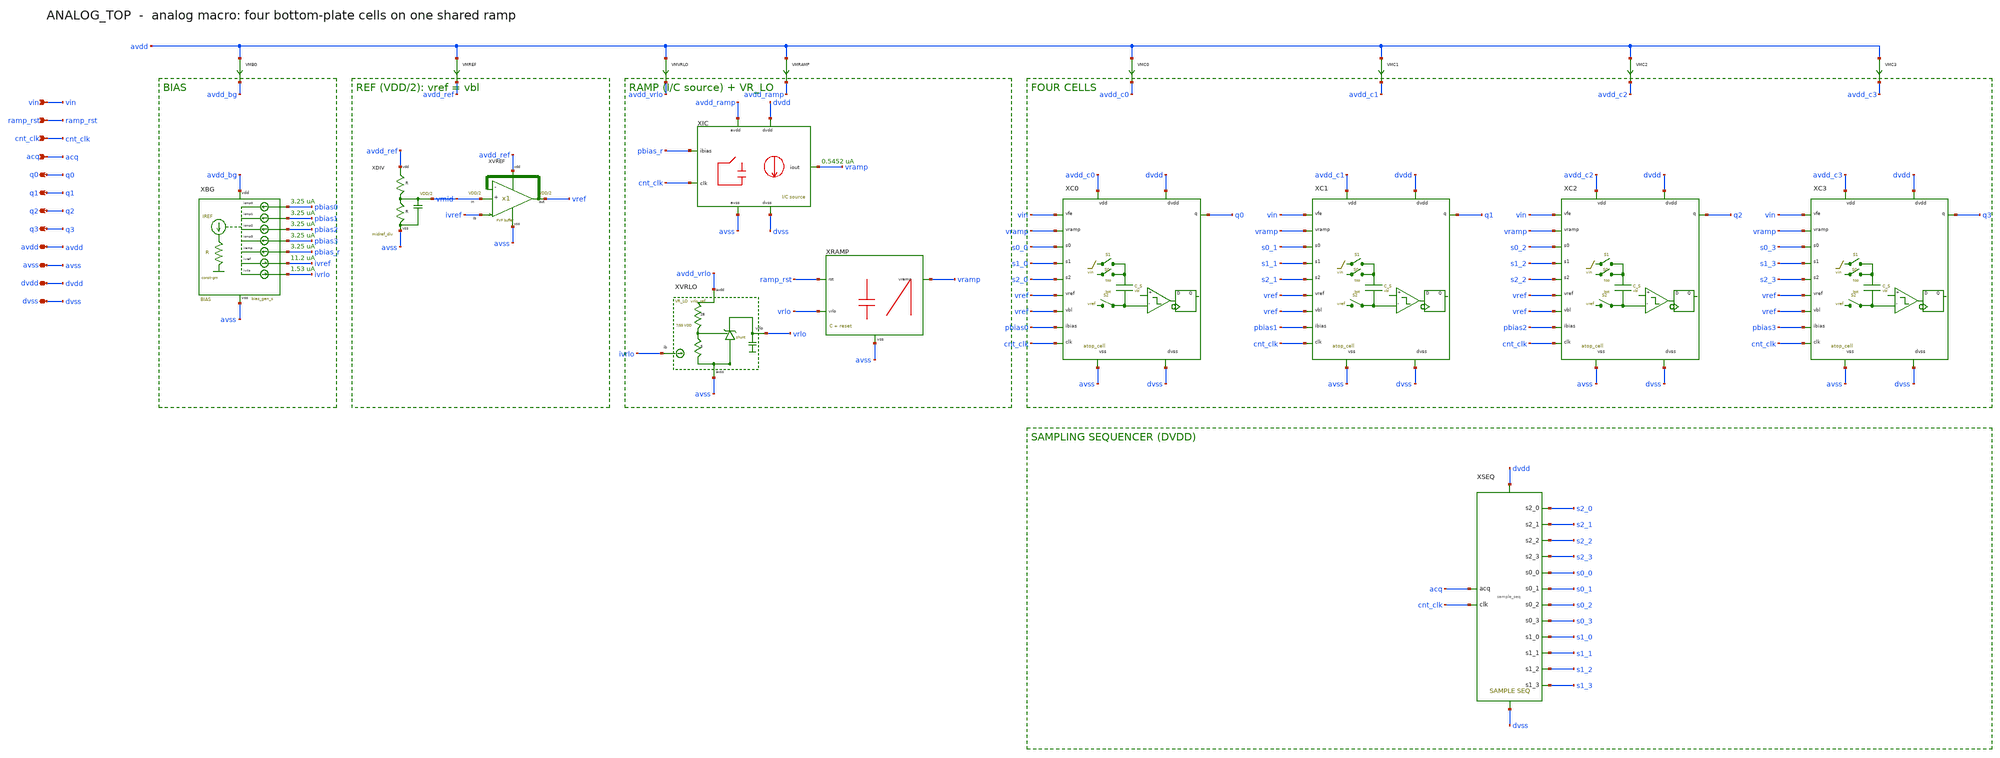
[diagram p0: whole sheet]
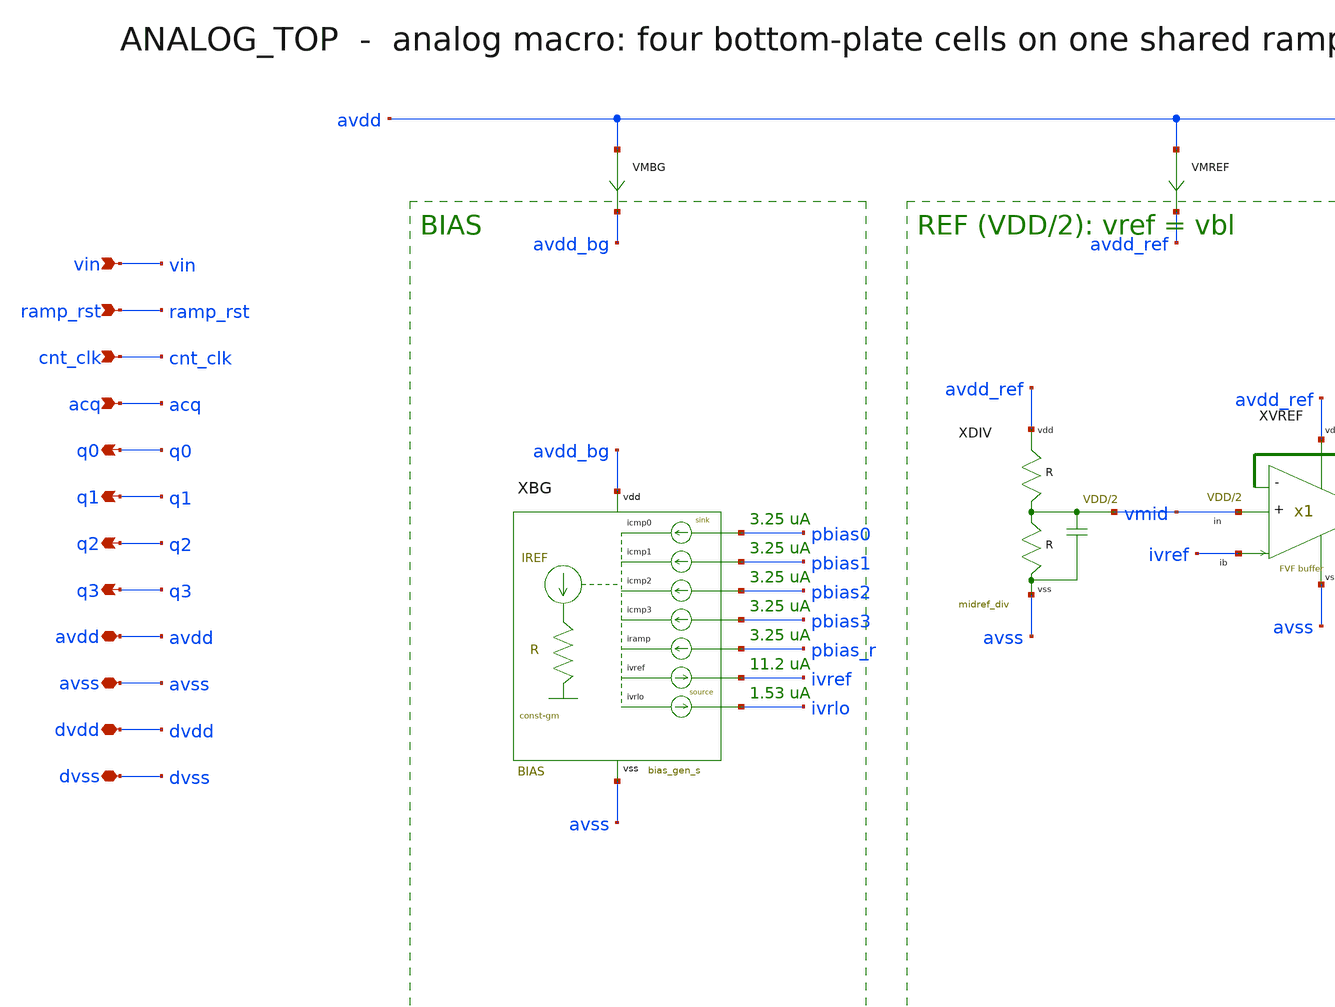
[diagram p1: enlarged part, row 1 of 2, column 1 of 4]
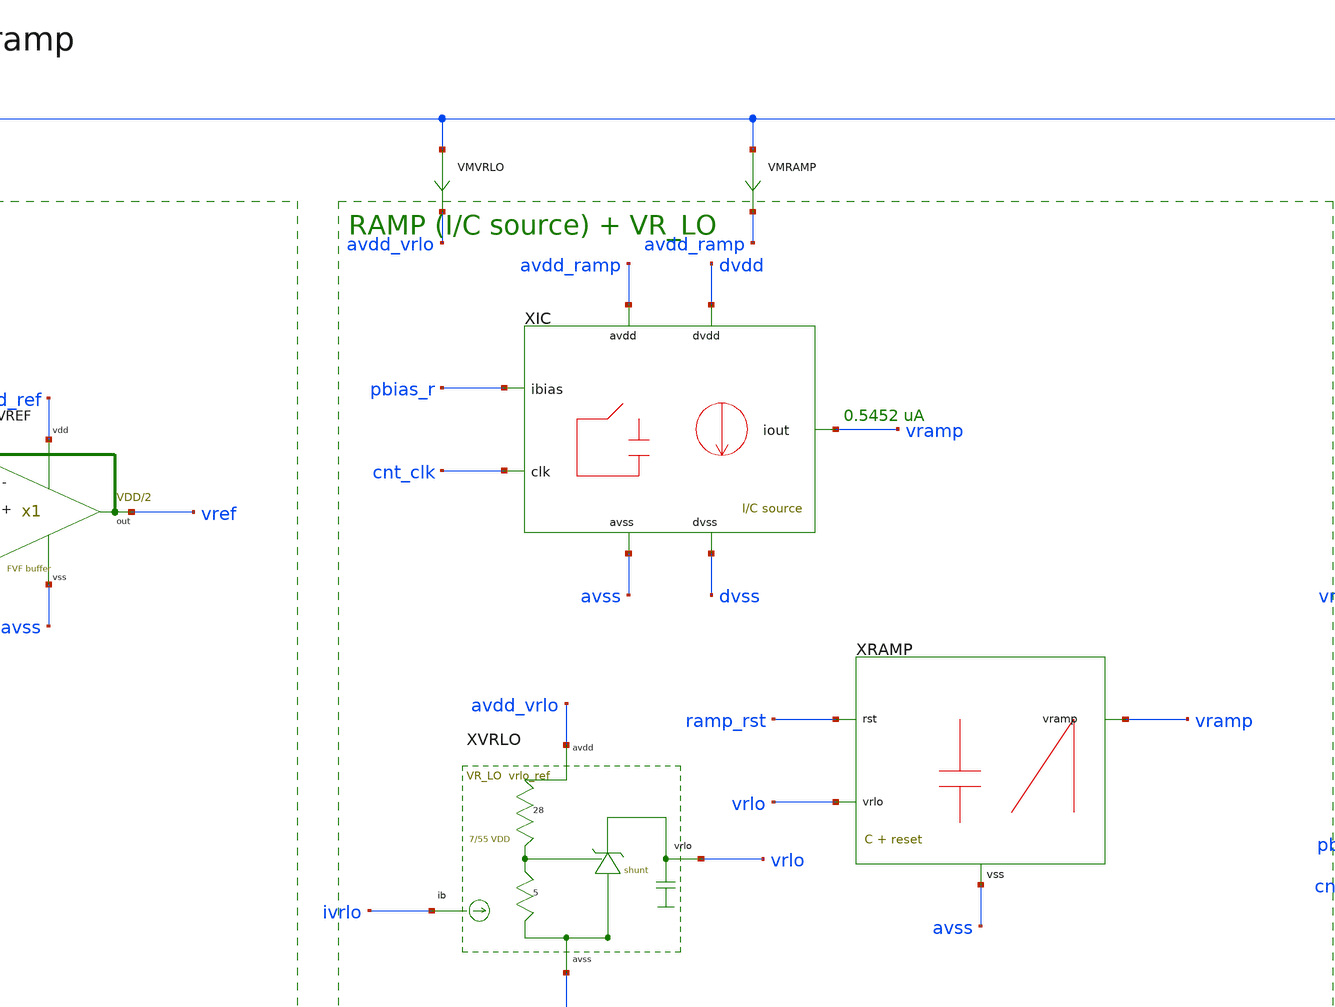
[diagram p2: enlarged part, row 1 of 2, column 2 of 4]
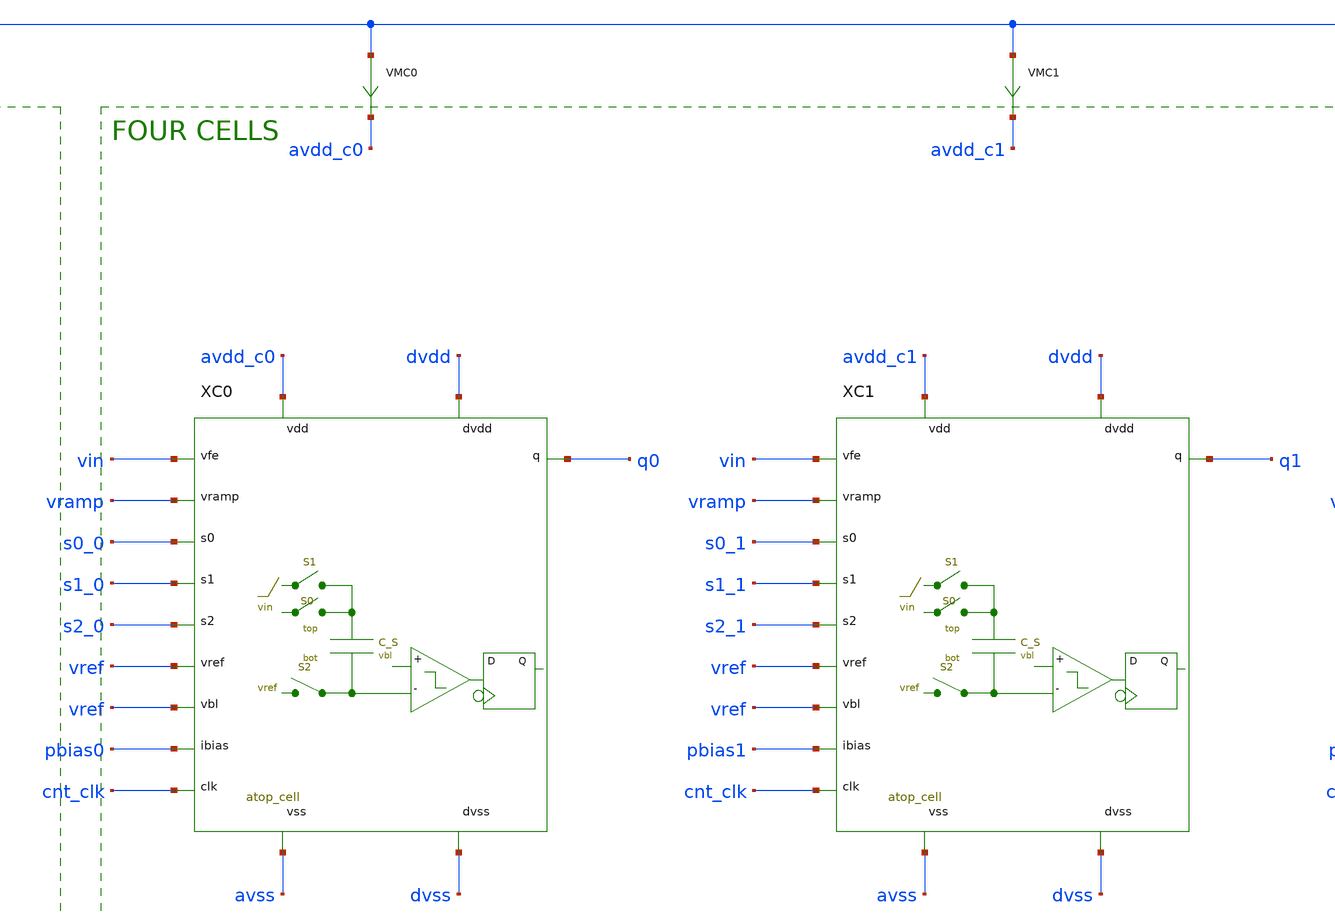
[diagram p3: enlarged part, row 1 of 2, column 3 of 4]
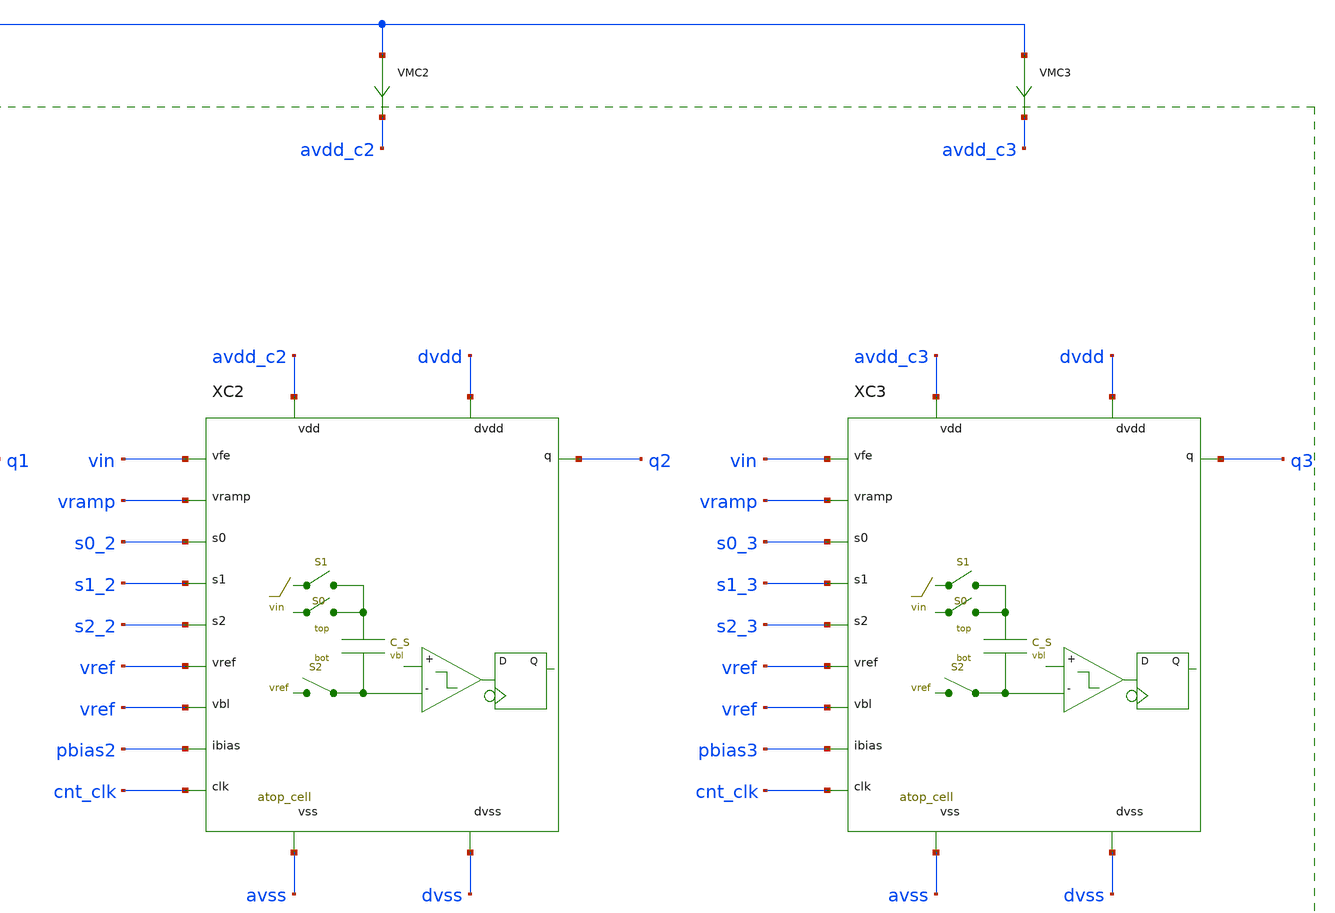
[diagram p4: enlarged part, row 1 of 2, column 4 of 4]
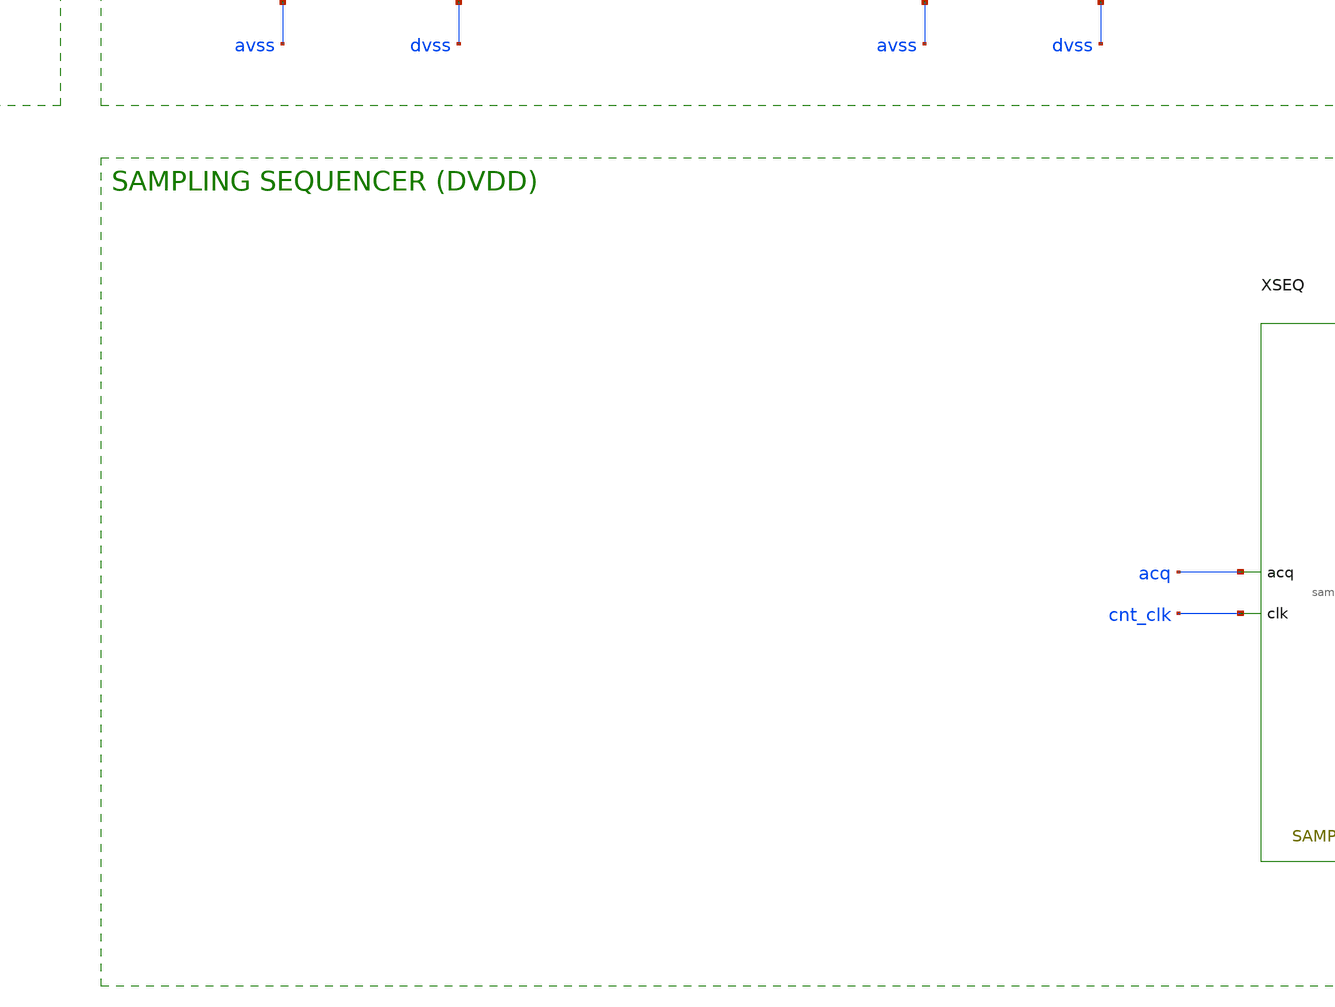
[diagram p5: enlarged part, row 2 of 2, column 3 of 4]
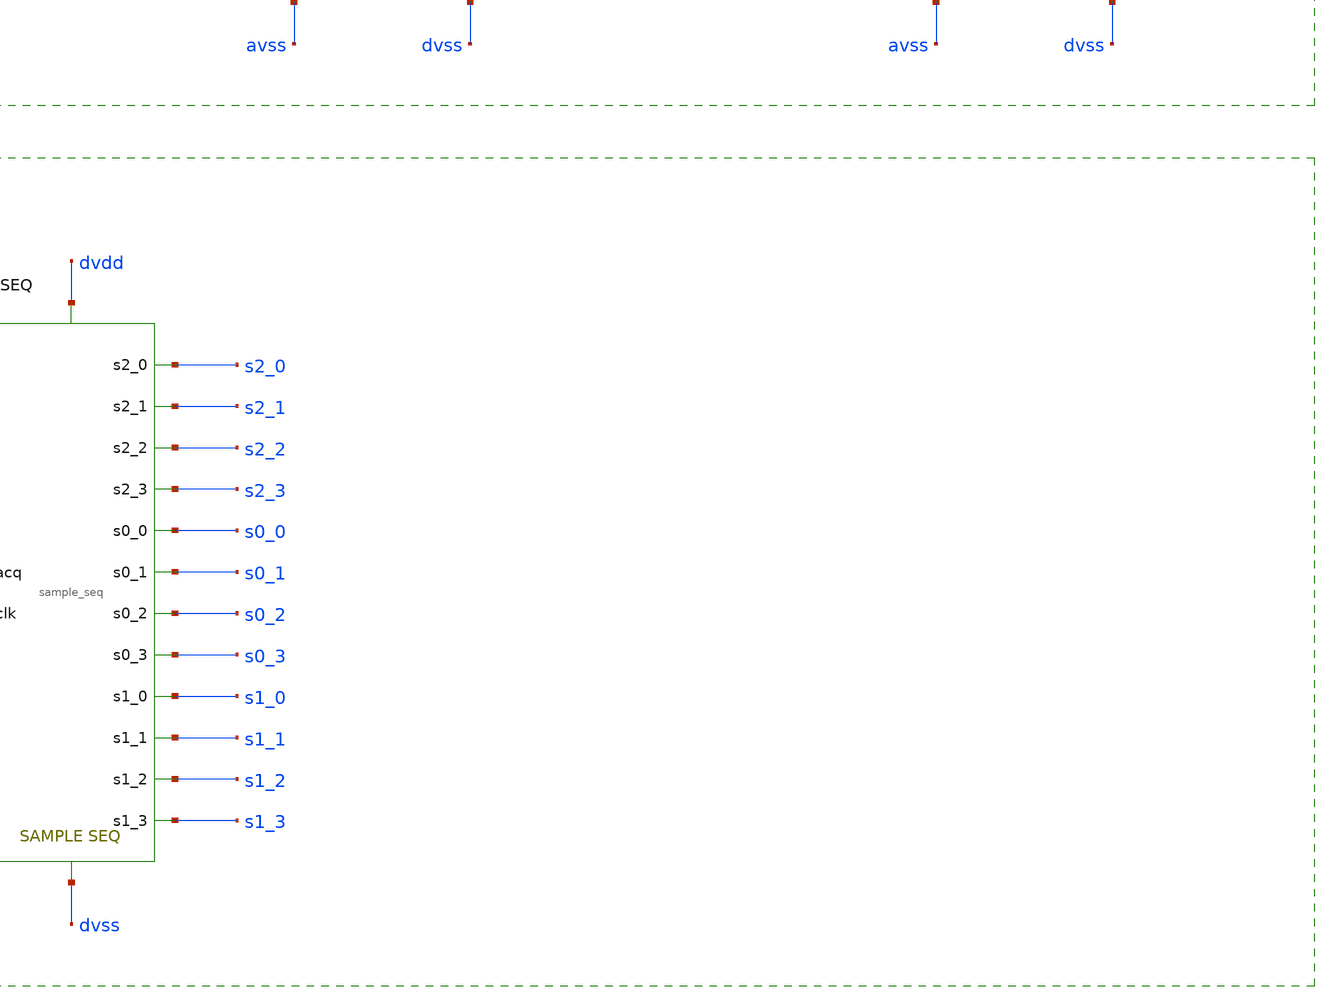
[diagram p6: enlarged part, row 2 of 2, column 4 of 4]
** sch_path: mixed_signal/Analog_top/analog_top.sch
**.subckt analog_top vin ramp_rst cnt_clk acq q0 q1 q2 q3 avdd avss dvdd dvss
*.ipin vin
*.ipin ramp_rst
*.ipin cnt_clk
*.ipin acq
*.opin q0
*.opin q1
*.opin q2
*.opin q3
*.iopin avdd
*.iopin avss
*.iopin dvdd
*.iopin dvss
VMBG avdd avdd_bg 0
VMREF avdd avdd_ref 0
VMVRLO avdd avdd_vrlo 0
VMRAMP avdd avdd_ramp 0
VMC0 avdd avdd_c0 0
VMC1 avdd avdd_c1 0
VMC2 avdd avdd_c2 0
VMC3 avdd avdd_c3 0
XBG avdd_bg avss pbias0 pbias1 pbias2 pbias3 pbias_r ivref ivrlo bias_gen_s
XDIV vmid avdd_ref avss midref_div
XVREF vref vmid ivref avdd_ref avss midref_buf
XVRLO vrlo ivrlo avdd_vrlo avss vrlo_ref
XIC vramp pbias_r cnt_clk avdd_ramp dvdd avss dvss ic_source
XRAMP vramp ramp_rst vrlo avss ramp_simple
XC0 vin vramp s0_0 s1_0 s2_0 vref vref pbias0 q0 cnt_clk avdd_c0 avss dvdd dvss atop_cell
XC1 vin vramp s0_1 s1_1 s2_1 vref vref pbias1 q1 cnt_clk avdd_c1 avss dvdd dvss atop_cell
XC2 vin vramp s0_2 s1_2 s2_2 vref vref pbias2 q2 cnt_clk avdd_c2 avss dvdd dvss atop_cell
XC3 vin vramp s0_3 s1_3 s2_3 vref vref pbias3 q3 cnt_clk avdd_c3 avss dvdd dvss atop_cell
XSEQ acq cnt_clk s2_0 s2_1 s2_2 s2_3 s0_0 s0_1 s0_2 s0_3 s1_0 s1_1 s1_2 s1_3 dvdd dvss sample_seq
**.ends
.end
